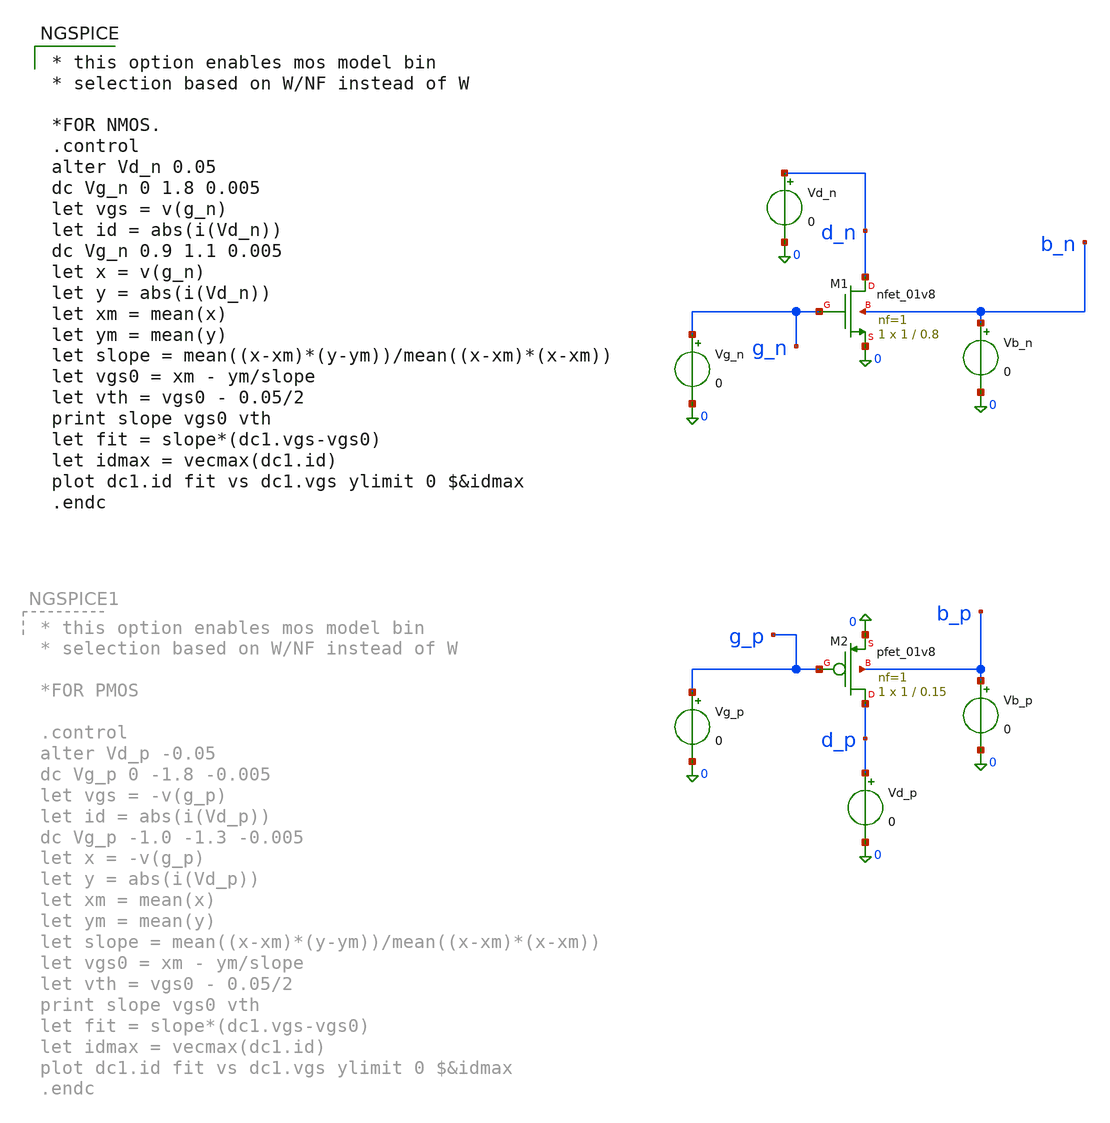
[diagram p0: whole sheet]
** sch_path: testcircuit/mos_parameter_extraction.sch
**.subckt mos_parameter_extraction
XM1 d_n g_n 0 b_n sky130_fd_pr__nfet_01v8 L=0.8 W=1 nf=1 ad='int((1 + 1)/2) * 1 / 1 * 0.29' as='int((1 + 2)/2) * 1 / 1 * 0.29'
+ pd='2*int((1 + 1)/2) * (1 / 1 + 0.29)' ps='2*int((1 + 2)/2) * (1 / 1 + 0.29)' nrd='0.29 / 1 ' nrs='0.29 / 1 '
+ sa=0 sb=0 sd=0 mult=1 m=1
XM2 d_p g_p 0 b_p sky130_fd_pr__pfet_01v8 L=0.15 W=1 nf=1 ad='int((1 + 1)/2) * 1 / 1 * 0.29' as='int((1 + 2)/2) * 1 / 1 * 0.29'
+ pd='2*int((1 + 1)/2) * (1 / 1 + 0.29)' ps='2*int((1 + 2)/2) * (1 / 1 + 0.29)' nrd='0.29 / 1 ' nrs='0.29 / 1 '
+ sa=0 sb=0 sd=0 mult=1 m=1
Vg_n g_n 0 0
Vd_n d_n 0 0
Vb_n b_n 0 0
Vg_p g_p 0 0
Vd_p d_p 0 0
Vb_p b_p 0 0
**** begin user architecture code

** opencircuitdesign pdks install
.lib $::SKYWATER_MODELS/sky130.lib.spice tt


* this option enables mos model bin
* selection based on W/NF instead of W

*FOR NMOS.
.control
alter Vd_n 0.05
dc Vg_n 0 1.8 0.005
let vgs = v(g_n)
let id = abs(i(Vd_n))
dc Vg_n 0.9 1.1 0.005
let x = v(g_n)
let y = abs(i(Vd_n))
let xm = mean(x)
let ym = mean(y)
let slope = mean((x-xm)*(y-ym))/mean((x-xm)*(x-xm))
let vgs0 = xm - ym/slope
let vth = vgs0 - 0.05/2
print slope vgs0 vth
let fit = slope*(dc1.vgs-vgs0)
let idmax = vecmax(dc1.id)
plot dc1.id fit vs dc1.vgs ylimit 0 $&idmax
.endc


**** end user architecture code
**.ends
.end
